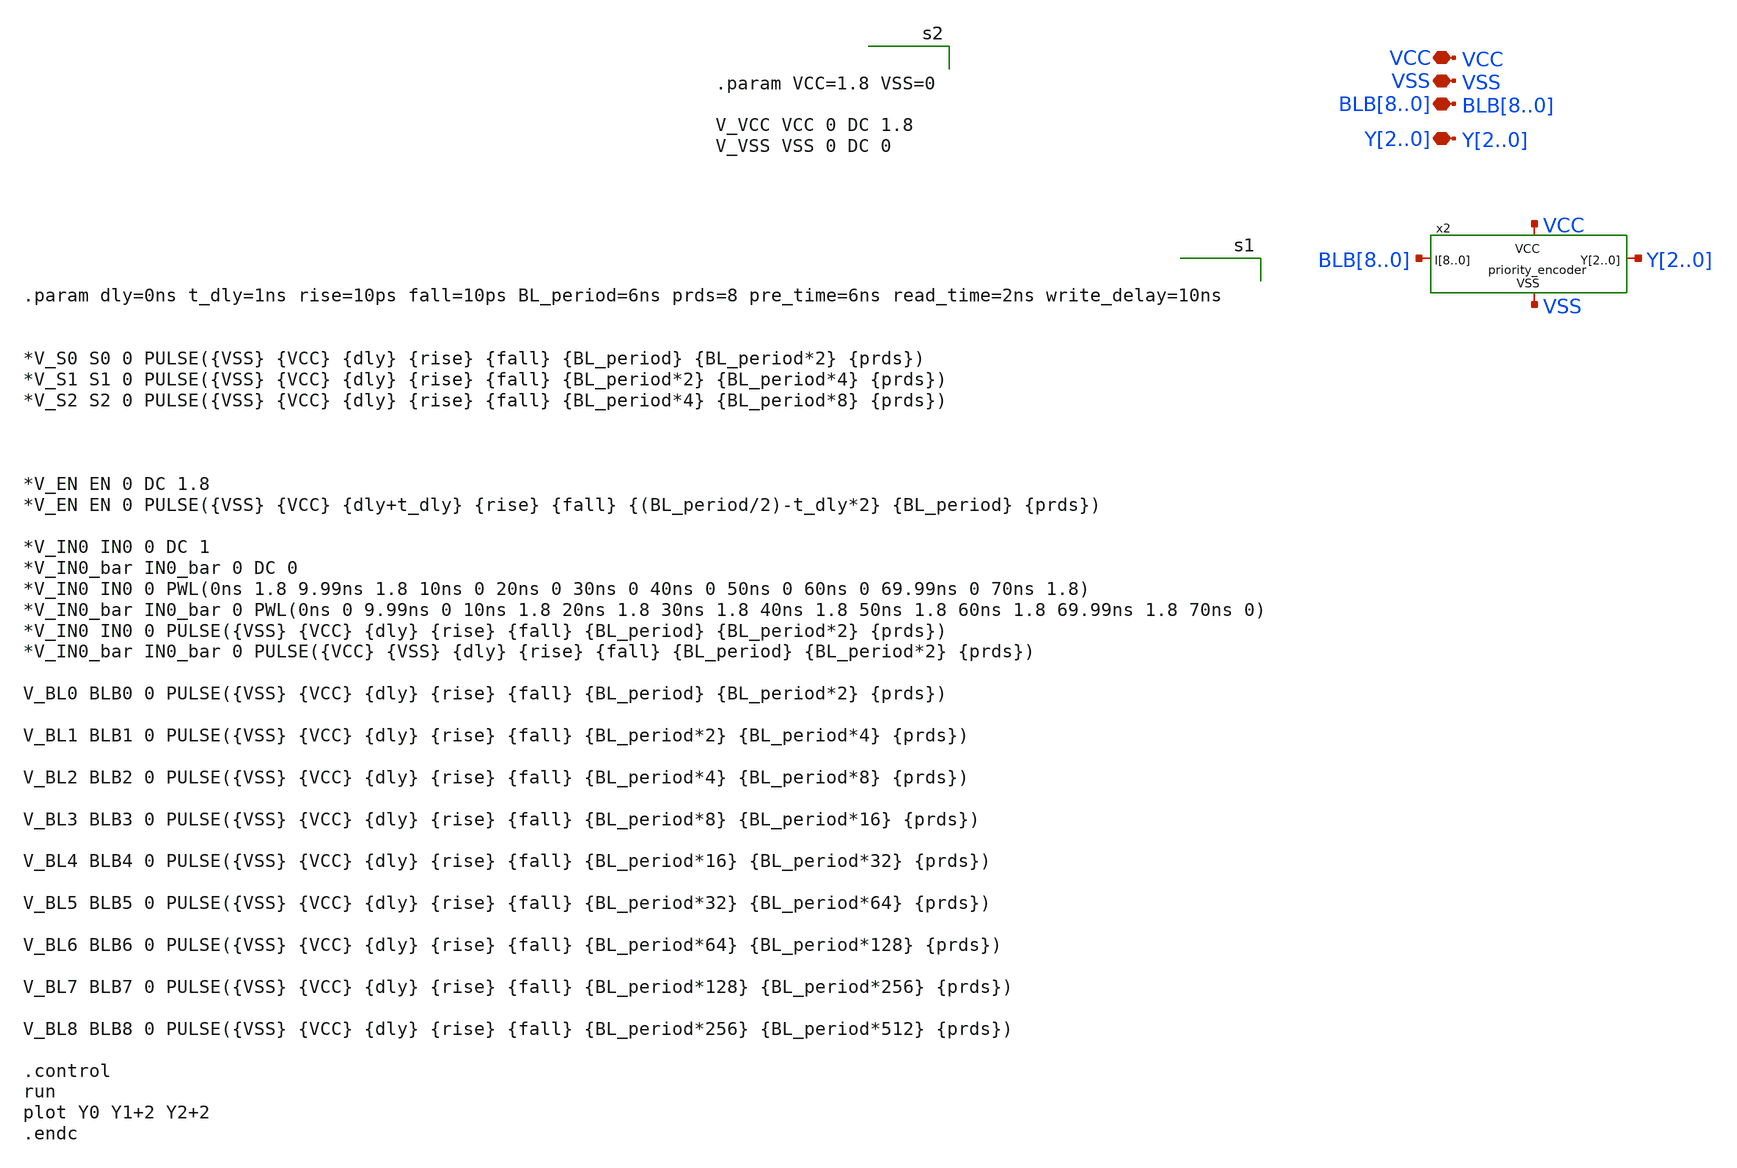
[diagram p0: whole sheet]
** sch_path: peripherals/priority_encoder_test.sch
**.subckt priority_encoder_test BLB8,BLB7,BLB6,BLB5,BLB4,BLB3,BLB2,BLB1,BLB0 VSS VCC Y2,Y1,Y0
*.iopin BLB8,BLB7,BLB6,BLB5,BLB4,BLB3,BLB2,BLB1,BLB0
*.iopin VSS
*.iopin VCC
*.iopin Y2,Y1,Y0
x2 VCC VSS BLB8 BLB7 BLB6 BLB5 BLB4 BLB3 BLB2 BLB1 BLB0 Y2 Y1 Y0 priority_encoder
**** begin user architecture code


.param dly=0ns t_dly=1ns rise=10ps fall=10ps BL_period=6ns prds=8 pre_time=6ns read_time=2ns
+ write_delay=10ns


*V_S0 S0 0 PULSE({VSS} {VCC} {dly} {rise} {fall} {BL_period} {BL_period*2} {prds})
*V_S1 S1 0 PULSE({VSS} {VCC} {dly} {rise} {fall} {BL_period*2} {BL_period*4} {prds})
*V_S2 S2 0 PULSE({VSS} {VCC} {dly} {rise} {fall} {BL_period*4} {BL_period*8} {prds})



*V_EN EN 0 DC 1.8
*V_EN EN 0 PULSE({VSS} {VCC} {dly+t_dly} {rise} {fall} {(BL_period/2)-t_dly*2} {BL_period} {prds})

*V_IN0 IN0 0 DC 1
*V_IN0_bar IN0_bar 0 DC 0
*V_IN0 IN0 0 PWL(0ns 1.8 9.99ns 1.8 10ns 0 20ns 0 30ns 0 40ns 0 50ns 0 60ns 0 69.99ns 0 70ns 1.8)
*V_IN0_bar IN0_bar 0 PWL(0ns 0 9.99ns 0 10ns 1.8 20ns 1.8 30ns 1.8 40ns 1.8 50ns 1.8 60ns 1.8
*+ 69.99ns 1.8 70ns 0)
*V_IN0 IN0 0 PULSE({VSS} {VCC} {dly} {rise} {fall} {BL_period} {BL_period*2} {prds})
*V_IN0_bar IN0_bar 0 PULSE({VCC} {VSS} {dly} {rise} {fall} {BL_period} {BL_period*2} {prds})

V_BL0 BLB0 0 PULSE({VSS} {VCC} {dly} {rise} {fall} {BL_period} {BL_period*2} {prds})

V_BL1 BLB1 0 PULSE({VSS} {VCC} {dly} {rise} {fall} {BL_period*2} {BL_period*4} {prds})

V_BL2 BLB2 0 PULSE({VSS} {VCC} {dly} {rise} {fall} {BL_period*4} {BL_period*8} {prds})

V_BL3 BLB3 0 PULSE({VSS} {VCC} {dly} {rise} {fall} {BL_period*8} {BL_period*16} {prds})

V_BL4 BLB4 0 PULSE({VSS} {VCC} {dly} {rise} {fall} {BL_period*16} {BL_period*32} {prds})

V_BL5 BLB5 0 PULSE({VSS} {VCC} {dly} {rise} {fall} {BL_period*32} {BL_period*64} {prds})

V_BL6 BLB6 0 PULSE({VSS} {VCC} {dly} {rise} {fall} {BL_period*64} {BL_period*128} {prds})

V_BL7 BLB7 0 PULSE({VSS} {VCC} {dly} {rise} {fall} {BL_period*128} {BL_period*256} {prds})

V_BL8 BLB8 0 PULSE({VSS} {VCC} {dly} {rise} {fall} {BL_period*256} {BL_period*512} {prds})

.control
run
plot Y0 Y1+2 Y2+2
.endc




** opencircuitdesign pdks install
.lib $::SKYWATER_MODELS/sky130.lib.spice tt



.param VCC=1.8 VSS=0

V_VCC VCC 0 DC 1.8
V_VSS VSS 0 DC 0


**** end user architecture code
**.ends
.end
